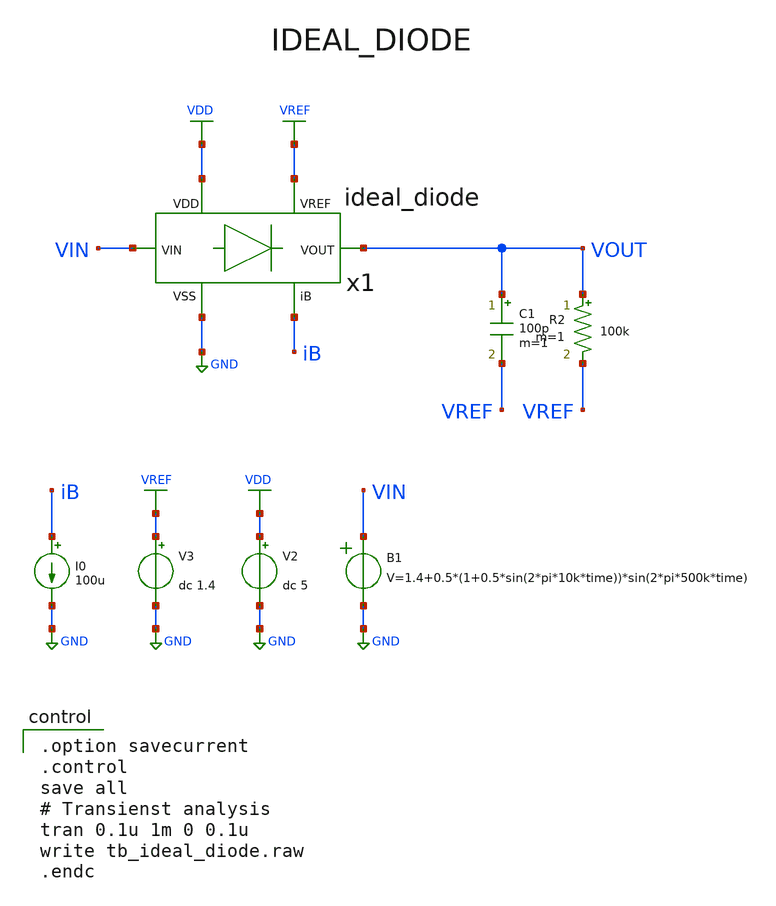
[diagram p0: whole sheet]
** sch_path: member_project/AM_Radio/Yamada3/xschem/tb_ideal_diode.sch
**.subckt tb_ideal_diode
V2 VDD GND dc 5
V3 VREF GND dc 1.4
B1 VIN GND V=1.4+0.5*(1+0.5*sin(2*pi*10k*time))*sin(2*pi*500k*time)
R2 VOUT VREF 100k m=1
x1 VDD GND VIN VOUT iB VREF ideal_diode
I0 iB GND 100u
C1 VOUT VREF 100p m=1
**** begin user architecture code
 .include $::LIB/ip62_models

.option savecurrent
.control
save all
# Transienst analysis
tran 0.1u 1m 0 0.1u
write tb_ideal_diode.raw
.endc

**** end user architecture code
**.ends
.GLOBAL GND
.GLOBAL VDD
.GLOBAL VREF
.end
